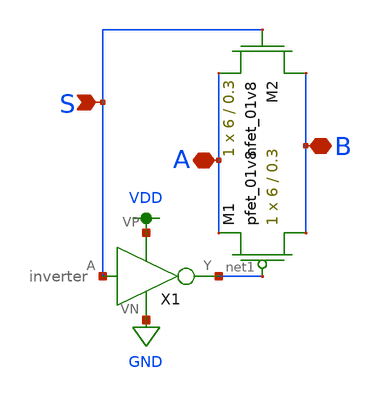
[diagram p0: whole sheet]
** sch_path: schematic/tg.sch
**.subckt tg S B A
*.ipin S
*.iopin B
*.iopin A
XM1 B net1 A VDD sky130_fd_pr__pfet_01v8 L=0.3 W=6 nf=1 ad='int((nf+1)/2) * W/nf * 0.29' as='int((nf+2)/2) * W/nf * 0.29'
+ pd='2*int((nf+1)/2) * (W/nf + 0.29)' ps='2*int((nf+2)/2) * (W/nf + 0.29)' nrd='0.29 / W' nrs='0.29 / W'
+ sa=0 sb=0 sd=0 mult=1 m=1
XM2 B S A GND sky130_fd_pr__nfet_01v8 L=0.3 W=6 nf=1 ad='int((nf+1)/2) * W/nf * 0.29' as='int((nf+2)/2) * W/nf * 0.29'
+ pd='2*int((nf+1)/2) * (W/nf + 0.29)' ps='2*int((nf+2)/2) * (W/nf + 0.29)' nrd='0.29 / W' nrs='0.29 / W'
+ sa=0 sb=0 sd=0 mult=1 m=1
X1 S GND VDD net1 inverter
**.ends

* expanding   symbol:
*+  /home/madvlsi/Documents/second/neuromorphic_computing_final/schematic/inverter.sym # of pins=4
** sym_path: schematic/inverter.sym
** sch_path: schematic/inverter.sch
.subckt inverter A VN VP Y
*.ipin A
*.iopin VP
*.iopin VN
*.opin Y
XM1 Y A VN VN sky130_fd_pr__nfet_01v8 L=0.15 W=1 nf=1 ad='int((nf+1)/2) * W/nf * 0.29' as='int((nf+2)/2) * W/nf * 0.29'
+ pd='2*int((nf+1)/2) * (W/nf + 0.29)' ps='2*int((nf+2)/2) * (W/nf + 0.29)' nrd='0.29 / W' nrs='0.29 / W'
+ sa=0 sb=0 sd=0 mult=1 m=1
XM2 Y A VP VP sky130_fd_pr__pfet_01v8 L=0.15 W=1 nf=1 ad='int((nf+1)/2) * W/nf * 0.29' as='int((nf+2)/2) * W/nf * 0.29'
+ pd='2*int((nf+1)/2) * (W/nf + 0.29)' ps='2*int((nf+2)/2) * (W/nf + 0.29)' nrd='0.29 / W' nrs='0.29 / W'
+ sa=0 sb=0 sd=0 mult=1 m=1
.ends

.GLOBAL VDD
.GLOBAL GND
.end
